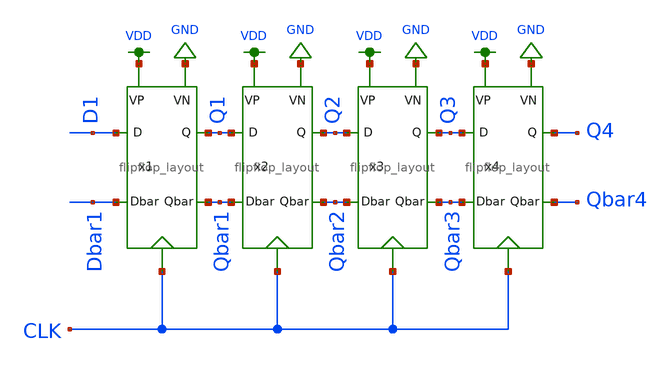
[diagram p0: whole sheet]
** sch_path: mp2/xschem/shiftregister/shift_register_lvs_noinverter.sch
**.subckt shift_register_lvs_noinverter
x1 D1 VDD Dbar1 GND Q1 CLK Qbar1 flipflop_layout
x2 Q1 VDD Qbar1 GND Q2 CLK Qbar2 flipflop_layout
x3 Q2 VDD Qbar2 GND Q3 CLK Qbar3 flipflop_layout
x4 Q3 VDD Qbar3 GND Q4 CLK Qbar4 flipflop_layout
**.ends
.GLOBAL GND
.GLOBAL VDD
.end
